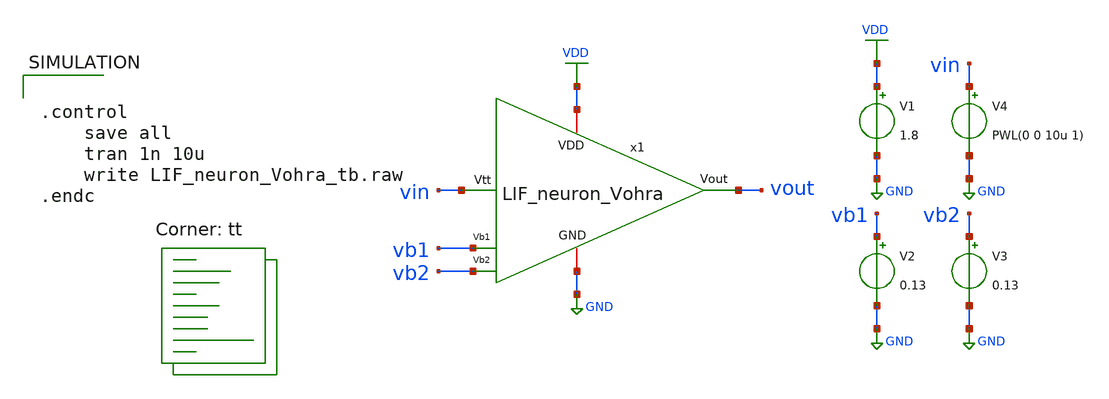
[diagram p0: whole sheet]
** sch_path: LIF_neuron/LIF_neuron_Vohra_tb.sch
**.subckt LIF_neuron_Vohra_tb
V1 VDD GND 1.8
V2 vb1 GND 0.13
V3 vb2 GND 0.13
V4 vin GND PWL(0 0 10u 1)
x1 VDD vout vb1 vin GND vb2 LIF_neuron_Vohra
**** begin user architecture code


.control
	save all
	tran 1n 10u
	write LIF_neuron_Vohra_tb.raw
.endc


.lib $::SKYWATER_MODELS/sky130.lib.spice tt

** opencircuitdesign pdks install
.inc $::SKYWATER_MODELS/rram_v0.spice

**** end user architecture code
**.ends

* expanding   symbol:  /home/ricardo/RATT_repos/Proyectos_xschem/LIF_neuron/LIF_neuron_Vohra.sym #
*+ of pins=6
** sym_path: LIF_neuron/LIF_neuron_Vohra.sym
** sch_path: LIF_neuron/LIF_neuron_Vohra.sch
.subckt LIF_neuron_Vohra VDD Vout Vb1 Vtt GND Vb2
*.ipin Vtt
*.iopin GND
*.ipin Vb1
*.ipin Vb2
*.iopin VDD
*.opin Vout
XM1 net4 Vtt GND GND sky130_fd_pr__nfet_01v8 L=0.4 W=0.24 nf=1 ad='int((nf+1)/2) * W/nf * 0.29' as='int((nf+2)/2) * W/nf * 0.29'
+ pd='2*int((nf+1)/2) * (W/nf + 0.29)' ps='2*int((nf+2)/2) * (W/nf + 0.29)' nrd='0.29 / W' nrs='0.29 / W'
+ sa=0 sb=0 sd=0 mult=1 m=1
XM3 net4 net4 VDD VDD sky130_fd_pr__pfet_01v8 L=0.4 W=0.24 nf=1 ad='int((nf+1)/2) * W/nf * 0.29' as='int((nf+2)/2) * W/nf * 0.29'
+ pd='2*int((nf+1)/2) * (W/nf + 0.29)' ps='2*int((nf+2)/2) * (W/nf + 0.29)' nrd='0.29 / W' nrs='0.29 / W'
+ sa=0 sb=0 sd=0 mult=1 m=1
XM13 net3 Vb1 GND GND sky130_fd_pr__nfet_01v8 L=0.2 W=2 nf=1 ad='int((nf+1)/2) * W/nf * 0.29' as='int((nf+2)/2) * W/nf * 0.29'
+ pd='2*int((nf+1)/2) * (W/nf + 0.29)' ps='2*int((nf+2)/2) * (W/nf + 0.29)' nrd='0.29 / W' nrs='0.29 / W'
+ sa=0 sb=0 sd=0 mult=1 m=1
XM12 net1 net2 net3 GND sky130_fd_pr__nfet_01v8 L=0.4 W=0.4 nf=1 ad='int((nf+1)/2) * W/nf * 0.29' as='int((nf+2)/2) * W/nf * 0.29'
+ pd='2*int((nf+1)/2) * (W/nf + 0.29)' ps='2*int((nf+2)/2) * (W/nf + 0.29)' nrd='0.29 / W' nrs='0.29 / W'
+ sa=0 sb=0 sd=0 mult=1 m=1
XM11 net1 net2 VDD VDD sky130_fd_pr__pfet_01v8 L=0.4 W=0.4 nf=1 ad='int((nf+1)/2) * W/nf * 0.29' as='int((nf+2)/2) * W/nf * 0.29'
+ pd='2*int((nf+1)/2) * (W/nf + 0.29)' ps='2*int((nf+2)/2) * (W/nf + 0.29)' nrd='0.29 / W' nrs='0.29 / W'
+ sa=0 sb=0 sd=0 mult=1 m=1
XC1 net1 GND sky130_fd_pr__cap_mim_m3_1 W=21 L=1 MF=1 m=1
XM14 net5 net1 GND GND sky130_fd_pr__nfet_01v8 L=0.4 W=0.4 nf=1 ad='int((nf+1)/2) * W/nf * 0.29' as='int((nf+2)/2) * W/nf * 0.29'
+ pd='2*int((nf+1)/2) * (W/nf + 0.29)' ps='2*int((nf+2)/2) * (W/nf + 0.29)' nrd='0.29 / W' nrs='0.29 / W'
+ sa=0 sb=0 sd=0 mult=1 m=1
XM4 net5 net4 VDD VDD sky130_fd_pr__pfet_01v8 L=0.4 W=0.4 nf=1 ad='int((nf+1)/2) * W/nf * 0.29' as='int((nf+2)/2) * W/nf * 0.29'
+ pd='2*int((nf+1)/2) * (W/nf + 0.29)' ps='2*int((nf+2)/2) * (W/nf + 0.29)' nrd='0.29 / W' nrs='0.29 / W'
+ sa=0 sb=0 sd=0 mult=1 m=1
XC2 net5 GND sky130_fd_pr__cap_mim_m3_1 W=10 L=1 MF=50 m=50
XM5 net5 Vb2 GND GND sky130_fd_pr__nfet_01v8 L=0.4 W=0.8 nf=1 ad='int((nf+1)/2) * W/nf * 0.29' as='int((nf+2)/2) * W/nf * 0.29'
+ pd='2*int((nf+1)/2) * (W/nf + 0.29)' ps='2*int((nf+2)/2) * (W/nf + 0.29)' nrd='0.29 / W' nrs='0.29 / W'
+ sa=0 sb=0 sd=0 mult=1 m=1
XM6 net6 Vout GND GND sky130_fd_pr__nfet_01v8 L=0.4 W=0.4 nf=1 ad='int((nf+1)/2) * W/nf * 0.29' as='int((nf+2)/2) * W/nf * 0.29'
+ pd='2*int((nf+1)/2) * (W/nf + 0.29)' ps='2*int((nf+2)/2) * (W/nf + 0.29)' nrd='0.29 / W' nrs='0.29 / W'
+ sa=0 sb=0 sd=0 mult=1 m=1
XM7 net2 net5 net6 GND sky130_fd_pr__nfet_01v8 L=0.4 W=0.4 nf=1 ad='int((nf+1)/2) * W/nf * 0.29' as='int((nf+2)/2) * W/nf * 0.29'
+ pd='2*int((nf+1)/2) * (W/nf + 0.29)' ps='2*int((nf+2)/2) * (W/nf + 0.29)' nrd='0.29 / W' nrs='0.29 / W'
+ sa=0 sb=0 sd=0 mult=1 m=1
XM8 net2 net5 VDD VDD sky130_fd_pr__pfet_01v8 L=0.4 W=0.4 nf=1 ad='int((nf+1)/2) * W/nf * 0.29' as='int((nf+2)/2) * W/nf * 0.29'
+ pd='2*int((nf+1)/2) * (W/nf + 0.29)' ps='2*int((nf+2)/2) * (W/nf + 0.29)' nrd='0.29 / W' nrs='0.29 / W'
+ sa=0 sb=0 sd=0 mult=1 m=1
XM9 Vout net2 net6 GND sky130_fd_pr__nfet_01v8 L=0.4 W=0.4 nf=1 ad='int((nf+1)/2) * W/nf * 0.29' as='int((nf+2)/2) * W/nf * 0.29'
+ pd='2*int((nf+1)/2) * (W/nf + 0.29)' ps='2*int((nf+2)/2) * (W/nf + 0.29)' nrd='0.29 / W' nrs='0.29 / W'
+ sa=0 sb=0 sd=0 mult=1 m=1
XM10 Vout net2 VDD VDD sky130_fd_pr__pfet_01v8 L=0.4 W=2 nf=1 ad='int((nf+1)/2) * W/nf * 0.29' as='int((nf+2)/2) * W/nf * 0.29'
+ pd='2*int((nf+1)/2) * (W/nf + 0.29)' ps='2*int((nf+2)/2) * (W/nf + 0.29)' nrd='0.29 / W' nrs='0.29 / W'
+ sa=0 sb=0 sd=0 mult=1 m=1
.ends

.GLOBAL GND
.GLOBAL VDD
.end
